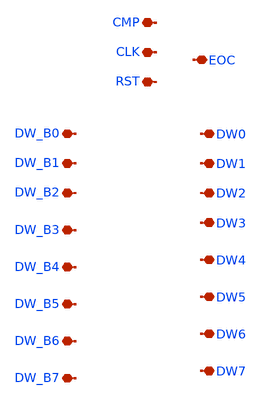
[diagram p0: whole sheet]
** sch_path: Designs/SAR_Logic.sch
**.subckt SAR_Logic DW0 DW1 DW2 DW3 DW4 DW5 DW6 DW7 DW_B0 DW_B1 DW_B2 DW_B3 DW_B4 DW_B5 DW_B6 DW_B7
*+ CMP CLK RST EOC
*.iopin DW0
*.iopin DW1
*.iopin DW2
*.iopin DW3
*.iopin DW4
*.iopin DW5
*.iopin DW6
*.iopin DW7
*.iopin DW_B0
*.iopin DW_B1
*.iopin DW_B2
*.iopin DW_B3
*.iopin DW_B4
*.iopin DW_B5
*.iopin DW_B6
*.iopin DW_B7
*.iopin CMP
*.iopin CLK
*.iopin RST
*.iopin EOC
**** begin user architecture code


a1 0 CLK RST 0 QCNT8 QCNT_B8 flop1
a2 QCNT8 CLK 0 RST QCNT7 QCNT_B7 flop1
a3 QCNT7 CLK 0 RST QCNT6 QCNT_B6 flop1
a4 QCNT6 CLK 0 RST QCNT5 QCNT_B5 flop1
a5 QCNT5 CLK 0 RST QCNT4 QCNT_B4 flop1
a6 QCNT4 CLK 0 RST QCNT3 QCNT_B3 flop1
a7 QCNT3 CLK 0 RST QCNT2 QCNT_B2 flop1
a8 QCNT2 CLK 0 RST QCNT1 QCNT_B1 flop1
a9 QCNT1 CLK 0 RST QCNT0 QCNT_B0 flop1
a10 CMP DW6 QCNT8 0 DW7 DW_B7 flop1
a11 CMP DW5 QCNT7 RST DW6 DW_B6 flop1
a12 CMP DW4 QCNT6 RST DW5 DW_B5 flop1
a13 CMP DW3 QCNT5 RST DW4 DW_B4 flop1
a14 CMP DW2 QCNT4 RST DW3 DW_B3 flop1
a15 CMP DW1 QCNT3 RST DW2 DW_B2 flop1
a16 CMP DW0 QCNT2 RST DW1 DW_B1 flop1
a17 CMP EOC QCNT1 RST DW0 DW_B0 flop1
a18 0 0 QCNT0 RST EOC NOOP flop1
.model flop1 d_dff(clk_delay = 10e-9 set_delay = 100e-12  reset_delay = 100e-12 ic =1.8 rise_delay =
+ 100e-12  fall_delay = 100e-12)


**** end user architecture code
**.ends
.end
